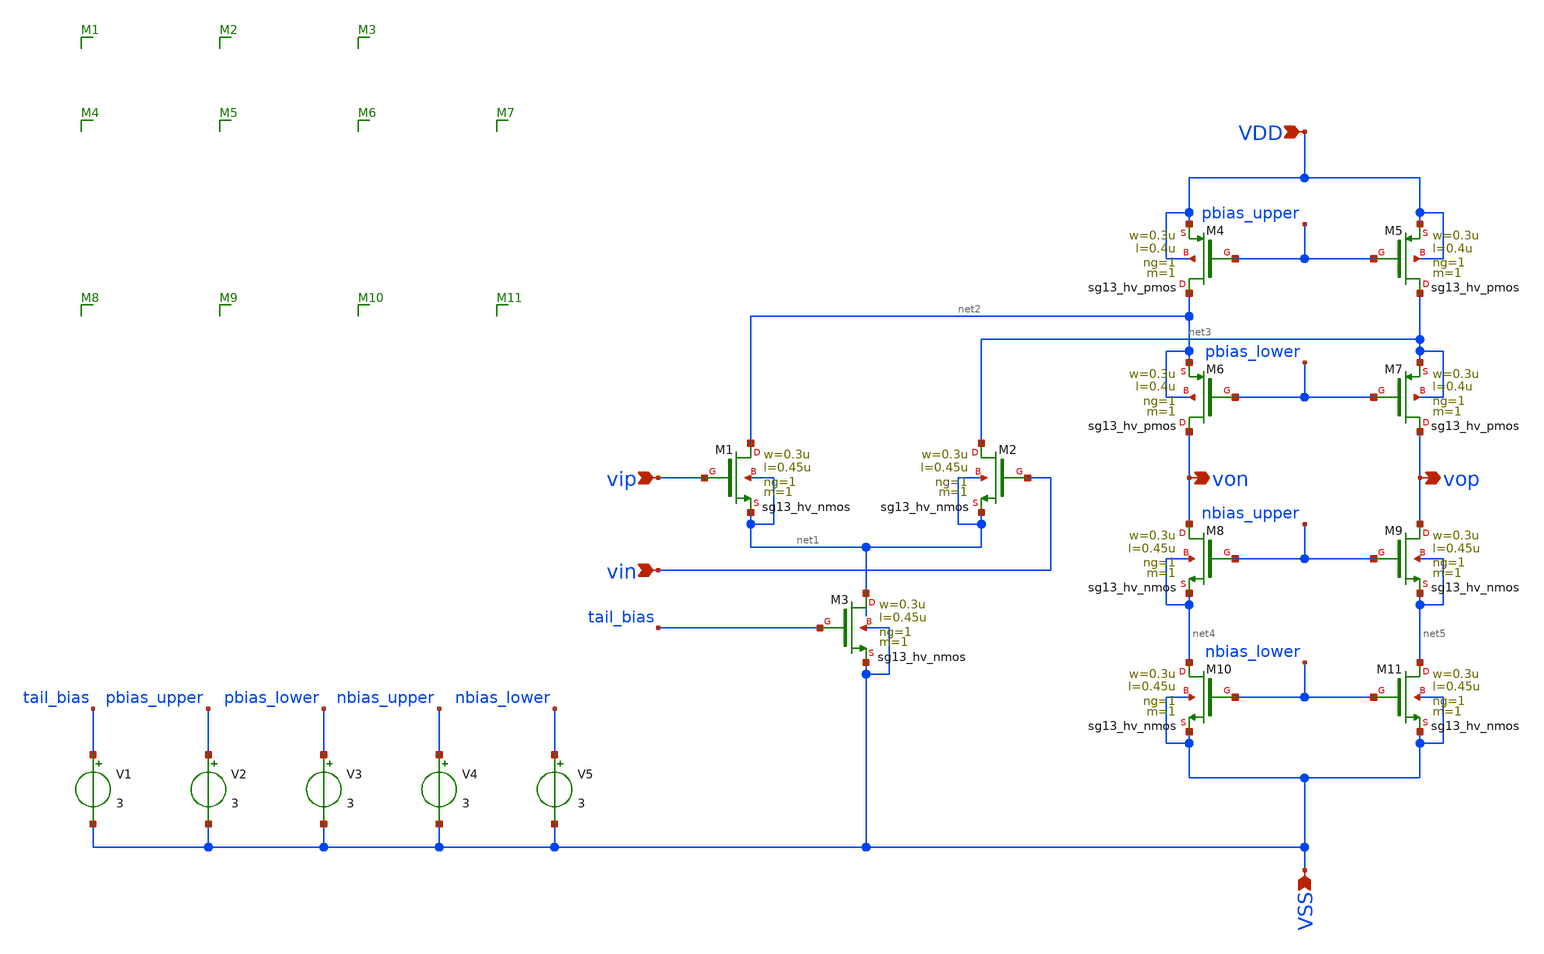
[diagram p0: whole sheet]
** sch_path: schematic/folded_cascode.sch
**.subckt folded_cascode VDD vip vin vop von VSS
*.ipin VDD
*.ipin vip
*.ipin vin
*.opin vop
*.opin von
*.ipin VSS
XM1 net2 vip net1 net1 sg13_hv_nmos w=0.3u l=0.45u ng=1 m=1 mm_ok=1
XM4 net2 pbias_upper VDD VDD sg13_hv_pmos w=0.3u l=0.4u ng=1 m=1 mm_ok=1
XM2 net3 vin net1 net1 sg13_hv_nmos w=0.3u l=0.45u ng=1 m=1 mm_ok=1
XM3 net1 tail_bias VSS VSS sg13_hv_nmos w=0.3u l=0.45u ng=1 m=1 mm_ok=1
XM5 net3 pbias_upper VDD VDD sg13_hv_pmos w=0.3u l=0.4u ng=1 m=1 mm_ok=1
XM6 von pbias_lower net2 net2 sg13_hv_pmos w=0.3u l=0.4u ng=1 m=1 mm_ok=1
XM7 vop pbias_lower net3 net3 sg13_hv_pmos w=0.3u l=0.4u ng=1 m=1 mm_ok=1
XM9 vop nbias_upper net5 net5 sg13_hv_nmos w=0.3u l=0.45u ng=1 m=1 mm_ok=1
XM8 von nbias_upper net4 net4 sg13_hv_nmos w=0.3u l=0.45u ng=1 m=1 mm_ok=1
XM11 net5 nbias_lower VSS VSS sg13_hv_nmos w=0.3u l=0.45u ng=1 m=1 mm_ok=1
XM10 net4 nbias_lower VSS VSS sg13_hv_nmos w=0.3u l=0.45u ng=1 m=1 mm_ok=1
V1 tail_bias VSS 3
V2 pbias_upper VSS 3
V3 pbias_lower VSS 3
V4 nbias_upper VSS 3
V5 nbias_lower VSS 3
**.ends
.end
